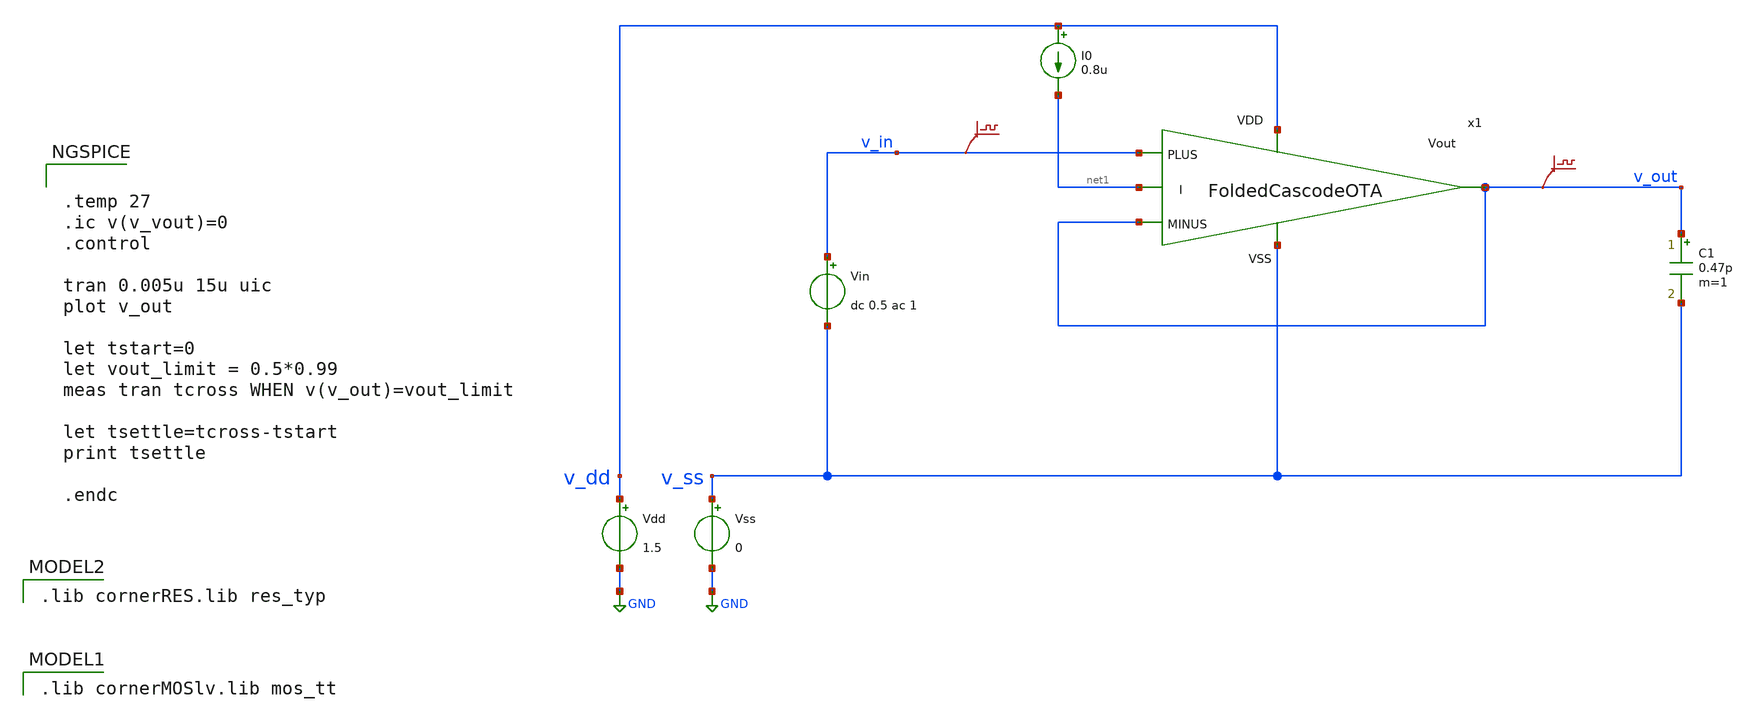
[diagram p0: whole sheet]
** sch_path: DSM/Schematics/Designs_Hrishi/RealCircuits/Folded Cascode/tb_FolCas_tran.sch
* (c) 2024 Hrishikesh, @HSB
**.subckt tb_FolCas_tran
Vdd v_dd GND 1.5
Vss v_ss GND 0
C1 v_out v_ss 0.47p m=1
Vin v_in v_ss dc 0.5 ac 1
I0 v_dd net1 0.8u
.save v(v_in)
.save v(v_out)
x1 v_dd net1 v_in v_out v_out v_ss FoldedCascodeOTA
**** begin user architecture code
 .lib cornerMOSlv.lib mos_tt

 .lib cornerRES.lib res_typ



.temp 27
.ic v(v_vout)=0
.control

tran 0.005u 15u uic
plot v_out

let tstart=0
let vout_limit = 0.5*0.99
meas tran tcross WHEN v(v_out)=vout_limit

let tsettle=tcross-tstart
print tsettle

.endc


**** end user architecture code
**.ends

* expanding   symbol:  /foss/designs/CEMS_DSM/DSM/Schematics/Designs_Hrishi/RealCircuits/Folded
*+ Cascode/FoldedCascodeOTA.sym # of pins=6
** sym_path: DSM/Schematics/IC_Designs_Hrishi/RealCircuits/Folded Cascode/FoldedCascodeOTA.sym
** sch_path: DSM/Schematics/IC_Designs_Hrishi/RealCircuits/Folded Cascode/FoldedCascodeOTA.sch
.subckt FoldedCascodeOTA VDD I PLUS MINUS Vout VSS
*.ipin PLUS
*.ipin MINUS
*.opin Vout
*.ipin VDD
*.ipin VSS
*.ipin I
XM1 net2 net4 VDD VDD sg13_lv_pmos w=0.272u l=0.5u ng=1 m=1 mm_ok=1
XM2 net1 PLUS net2 VDD sg13_lv_pmos w=0.136u l=0.5u ng=1 m=1 mm_ok=1
XM3 net6 MINUS net2 VDD sg13_lv_pmos w=0.136u l=0.5u ng=1 m=1 mm_ok=1
XM14 net6 net9 VSS VSS sg13_lv_nmos w=0.30u l=2u ng=1 m=1 mm_ok=1
XM13 Vout I net6 VSS sg13_lv_nmos w=0.15u l=2u ng=1 m=1 mm_ok=1
XM11 net7 I net1 VSS sg13_lv_nmos w=0.15u l=2u ng=1 m=1 mm_ok=1
XM12 net1 net9 VSS VSS sg13_lv_nmos w=0.30u l=2u ng=1 m=1 mm_ok=1
XM5 Vout net3 net5 VDD sg13_lv_pmos w=0.136u l=0.5u ng=1 m=1 mm_ok=1
XM4 net5 net4 VDD VDD sg13_lv_pmos w=0.136u l=0.5u ng=1 m=1 mm_ok=1
XM6 net4 net4 VDD VDD sg13_lv_pmos w=0.136u l=0.5u ng=1 m=1 mm_ok=1
XM8 net3 net3 net4 VDD sg13_lv_pmos w=0.136u l=0.5u ng=1 m=1 mm_ok=1
XM9 net8 net4 VDD VDD sg13_lv_pmos w=0.136u l=0.5u ng=1 m=1 mm_ok=1
XM10 net7 net3 net8 VDD sg13_lv_pmos w=0.136u l=0.5u ng=1 m=1 mm_ok=1
XM16 I I net9 VSS sg13_lv_nmos w=0.15u l=2u ng=1 m=1 mm_ok=1
XM15 net9 net9 VSS VSS sg13_lv_nmos w=0.15u l=2u ng=1 m=1 mm_ok=1
XM7 net3 net9 VSS VSS sg13_lv_nmos w=0.15u l=2u ng=1 m=1 mm_ok=1
XM18 VDD I net10 VSS sg13_lv_nmos w=0.15u l=2u ng=1 m=1 mm_ok=1
XM17 net10 net9 VSS VSS sg13_lv_nmos w=0.15u l=2u ng=1 m=1 mm_ok=1
.ends

.GLOBAL GND
.end
